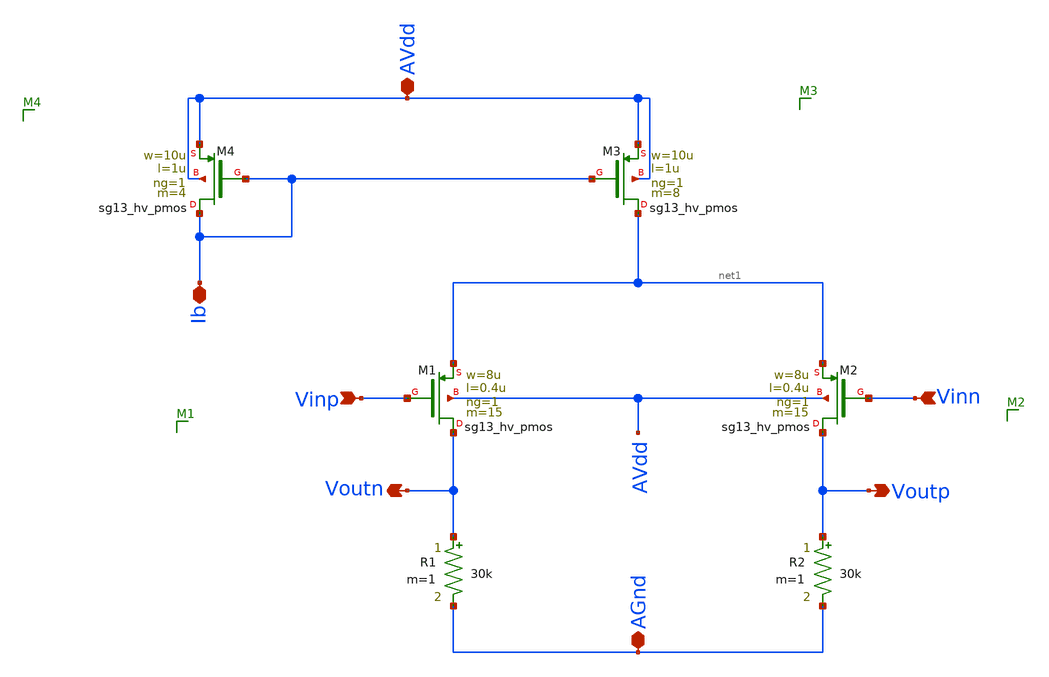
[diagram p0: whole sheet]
** sch_path: Schematics/lab_5/diff_amp.sch
**.subckt diff_amp Vinp Vinn Voutn Voutp AVdd AGnd Ib
*.ipin Vinp
*.ipin Vinn
*.opin Voutn
*.opin Voutp
*.iopin AVdd
*.iopin AGnd
*.iopin Ib
XM1 Voutn Vinp net1 AVdd sg13_hv_pmos w=8u l=0.4u ng=1 m=15 mm_ok=1
XM2 Voutp Vinn net1 AVdd sg13_hv_pmos w=8u l=0.4u ng=1 m=15 mm_ok=1
R1 Voutn AGnd 30k m=1
R2 Voutp AGnd 30k m=1
XM3 net1 Ib AVdd AVdd sg13_hv_pmos w=10u l=1u ng=1 m=8 mm_ok=1
XM4 Ib Ib AVdd AVdd sg13_hv_pmos w=10u l=1u ng=1 m=4 mm_ok=1
**.ends
.end
